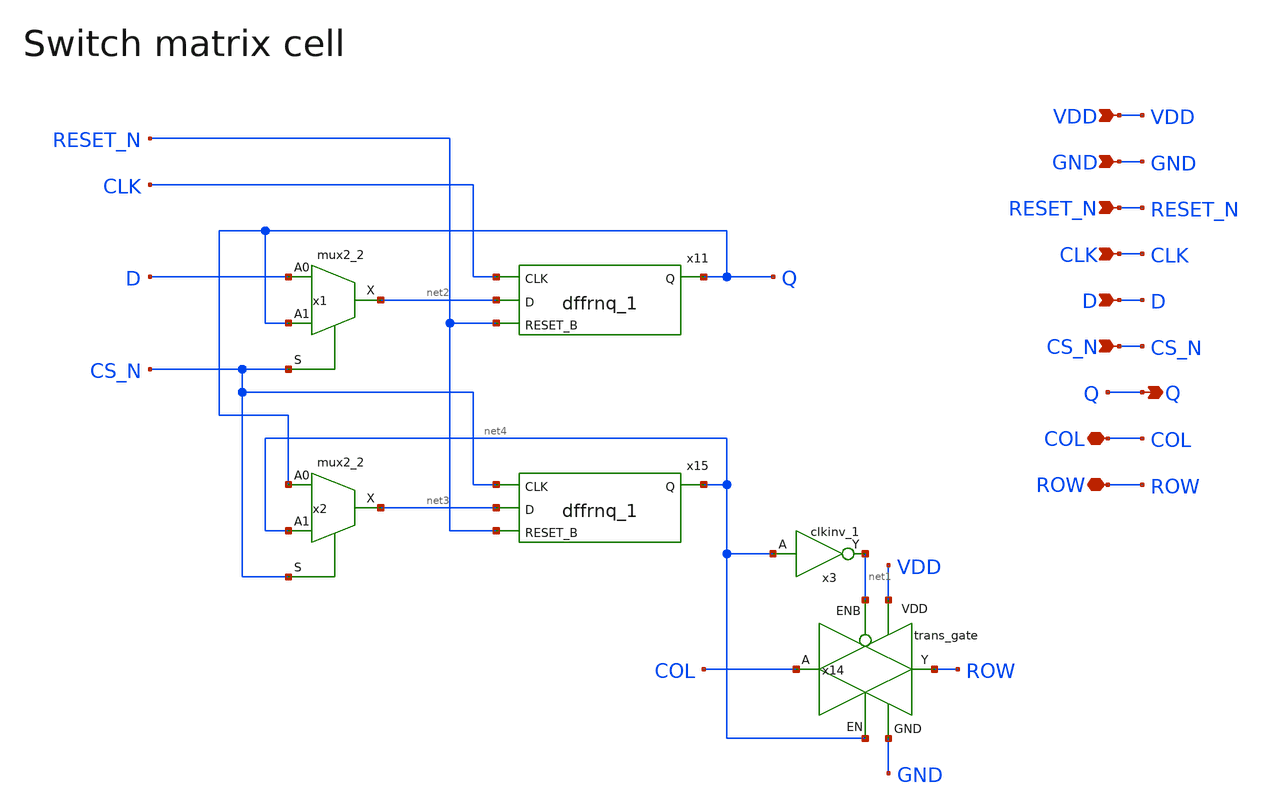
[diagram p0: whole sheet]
** sch_path: designs/libs/core_analog/sw_matrix/sw_matrix_cell.sch
* Copyright 2022 GlobalFoundries PDK Authors
* Licensed under the Apache License, Version 2.0 (the "License");
* you may not use this file except in compliance with the License.
* You may obtain a copy of the License at
* https://www.apache.org/licenses/LICENSE-2.0
* Unless required by applicable law or agreed to in writing, software
* distributed under the License is distributed on an "AS IS" BASIS,
* WITHOUT WARRANTIES OR CONDITIONS OF ANY KIND, either express or implied.
* See the License for the specific language governing permissions and
* limitations under the License.
**.subckt sw_matrix_cell RESET_N CLK D CS_N GND VDD Q COL ROW
*.ipin RESET_N
*.ipin CLK
*.ipin D
*.ipin CS_N
*.ipin GND
*.ipin VDD
*.opin Q
*.iopin COL
*.iopin ROW
x11 net2 RESET_N CLK Q VDD VDD GND GND gf180mcu_fd_sc_mcu7t5v0__dffrnq_1
x14 VDD GND COL net1 ROW net4 trans_gate
x15 net3 RESET_N CS_N net4 VDD VDD GND GND gf180mcu_fd_sc_mcu7t5v0__dffrnq_1
x1 D Q CS_N net2 VPWR VNB VPB VGND gf180mcu_fd_sc_mcu7t5v0__mux2_2
x2 Q net4 CS_N net3 VPWR VNB VPB VGND gf180mcu_fd_sc_mcu7t5v0__mux2_2
x3 net4 net1 VDD VDD GND GND gf180mcu_fd_sc_mcu7t5v0__clkinv_1
**.ends
.end
